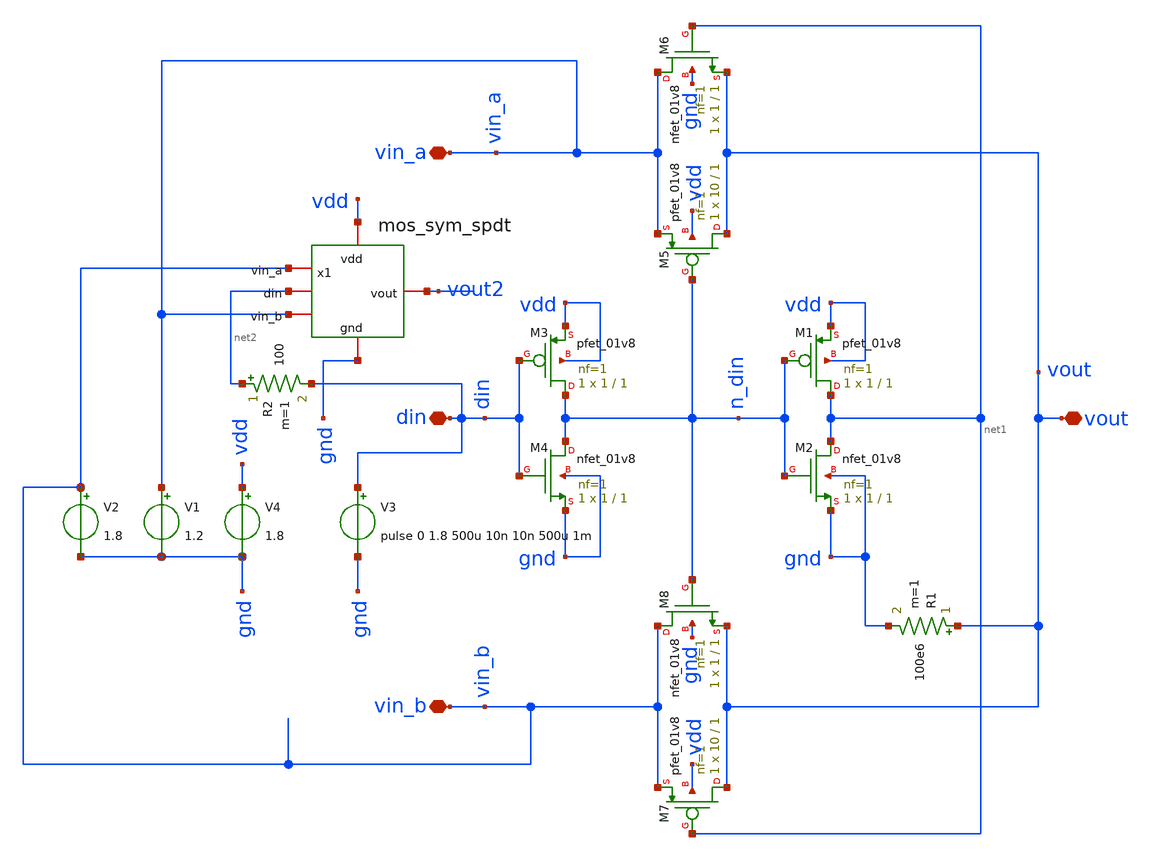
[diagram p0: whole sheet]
** sch_path: Schematics/mos_spdt.sch
**.subckt mos_spdt vout vin_a vin_b din
*.iopin vout
*.iopin vin_a
*.iopin vin_b
*.iopin din
XM3 n_din din vdd vdd sky130_fd_pr__pfet_01v8 L=1 W=1 nf=1 ad='int((nf+1)/2) * W/nf * 0.29' as='int((nf+2)/2) * W/nf * 0.29'
+ pd='2*int((nf+1)/2) * (W/nf + 0.29)' ps='2*int((nf+2)/2) * (W/nf + 0.29)' nrd='0.29 / W' nrs='0.29 / W'
+ sa=0 sb=0 sd=0 mult=1 m=1
XM4 n_din din gnd gnd sky130_fd_pr__nfet_01v8 L=1 W=1 nf=1 ad='int((1 + 1)/2) * 1 / 1 * 0.29' as='int((1 + 2)/2) * 1 / 1 * 0.29'
+ pd='2*int((1 + 1)/2) * (1 / 1 + 0.29)' ps='2*int((1 + 2)/2) * (1 / 1 + 0.29)' nrd='0.29 / 1 ' nrs='0.29 / 1 '
+ sa=0 sb=0 sd=0 mult=1 m=1
XM1 net1 n_din vdd vdd sky130_fd_pr__pfet_01v8 L=1 W=1 nf=1 ad='int((nf+1)/2) * W/nf * 0.29' as='int((nf+2)/2) * W/nf * 0.29'
+ pd='2*int((nf+1)/2) * (W/nf + 0.29)' ps='2*int((nf+2)/2) * (W/nf + 0.29)' nrd='0.29 / W' nrs='0.29 / W'
+ sa=0 sb=0 sd=0 mult=1 m=1
XM2 net1 n_din gnd gnd sky130_fd_pr__nfet_01v8 L=1 W=1 nf=1 ad='int((1 + 1)/2) * 1 / 1 * 0.29' as='int((1 + 2)/2) * 1 / 1 * 0.29'
+ pd='2*int((1 + 1)/2) * (1 / 1 + 0.29)' ps='2*int((1 + 2)/2) * (1 / 1 + 0.29)' nrd='0.29 / 1 ' nrs='0.29 / 1 '
+ sa=0 sb=0 sd=0 mult=1 m=1
XM5 vout n_din vin_a vdd sky130_fd_pr__pfet_01v8 L=1 W=10 nf=1 ad='int((nf+1)/2) * W/nf * 0.29' as='int((nf+2)/2) * W/nf * 0.29'
+ pd='2*int((nf+1)/2) * (W/nf + 0.29)' ps='2*int((nf+2)/2) * (W/nf + 0.29)' nrd='0.29 / W' nrs='0.29 / W'
+ sa=0 sb=0 sd=0 mult=1 m=1
XM6 vin_a net1 vout gnd sky130_fd_pr__nfet_01v8 L=1 W=1 nf=1 ad='int((1 + 1)/2) * 1 / 1 * 0.29' as='int((1 + 2)/2) * 1 / 1 * 0.29'
+ pd='2*int((1 + 1)/2) * (1 / 1 + 0.29)' ps='2*int((1 + 2)/2) * (1 / 1 + 0.29)' nrd='0.29 / 1 ' nrs='0.29 / 1 '
+ sa=0 sb=0 sd=0 mult=1 m=1
XM7 vout net1 vin_b vdd sky130_fd_pr__pfet_01v8 L=1 W=10 nf=1 ad='int((nf+1)/2) * W/nf * 0.29' as='int((nf+2)/2) * W/nf * 0.29'
+ pd='2*int((nf+1)/2) * (W/nf + 0.29)' ps='2*int((nf+2)/2) * (W/nf + 0.29)' nrd='0.29 / W' nrs='0.29 / W'
+ sa=0 sb=0 sd=0 mult=1 m=1
XM8 vin_b n_din vout gnd sky130_fd_pr__nfet_01v8 L=1 W=1 nf=1 ad='int((1 + 1)/2) * 1 / 1 * 0.29' as='int((1 + 2)/2) * 1 / 1 * 0.29'
+ pd='2*int((1 + 1)/2) * (1 / 1 + 0.29)' ps='2*int((1 + 2)/2) * (1 / 1 + 0.29)' nrd='0.29 / 1 ' nrs='0.29 / 1 '
+ sa=0 sb=0 sd=0 mult=1 m=1
V3 din gnd pulse 0 1.8 500u 10n 10n 500u 1m
V4 vdd gnd 1.8
V1 vin_a gnd 1.2
V2 vin_b gnd 1.8
R1 vout gnd 100e6 m=1
x1 vdd vin_b vout2 net2 vin_a gnd mos_sym_spdt
R2 net2 din 100 m=1
**** begin user architecture code

** opencircuitdesign pdks install
.lib $::SKYWATER_MODELS/sky130.lib.spice tt


**** end user architecture code
**.ends

* expanding   symbol:  Symbols/mos_sym_spdt.sym # of pins=6
** sym_path: Symbols/mos_sym_spdt.sym
** sch_path: Symbols/mos_sym_spdt.sch
.subckt mos_sym_spdt vdd vin_a vout din vin_b gnd
*.iopin vout
*.iopin vin_a
*.iopin vin_b
*.iopin vdd
*.iopin gnd
*.ipin din
XM3 n_din din vdd vdd sky130_fd_pr__pfet_01v8 L=1 W=1 nf=1 ad='int((nf+1)/2) * W/nf * 0.29' as='int((nf+2)/2) * W/nf * 0.29'
+ pd='2*int((nf+1)/2) * (W/nf + 0.29)' ps='2*int((nf+2)/2) * (W/nf + 0.29)' nrd='0.29 / W' nrs='0.29 / W'
+ sa=0 sb=0 sd=0 mult=1 m=1
XM4 n_din din net1 net1 sky130_fd_pr__nfet_01v8 L=1 W=1 nf=1 ad='int((1 + 1)/2) * 1 / 1 * 0.29' as='int((1 + 2)/2) * 1 / 1 * 0.29'
+ pd='2*int((1 + 1)/2) * (1 / 1 + 0.29)' ps='2*int((1 + 2)/2) * (1 / 1 + 0.29)' nrd='0.29 / 1 ' nrs='0.29 / 1 '
+ sa=0 sb=0 sd=0 mult=1 m=1
XM1 net2 n_din vdd vdd sky130_fd_pr__pfet_01v8 L=1 W=1 nf=1 ad='int((nf+1)/2) * W/nf * 0.29' as='int((nf+2)/2) * W/nf * 0.29'
+ pd='2*int((nf+1)/2) * (W/nf + 0.29)' ps='2*int((nf+2)/2) * (W/nf + 0.29)' nrd='0.29 / W' nrs='0.29 / W'
+ sa=0 sb=0 sd=0 mult=1 m=1
XM2 net2 n_din gnd gnd sky130_fd_pr__nfet_01v8 L=1 W=1 nf=1 ad='int((1 + 1)/2) * 1 / 1 * 0.29' as='int((1 + 2)/2) * 1 / 1 * 0.29'
+ pd='2*int((1 + 1)/2) * (1 / 1 + 0.29)' ps='2*int((1 + 2)/2) * (1 / 1 + 0.29)' nrd='0.29 / 1 ' nrs='0.29 / 1 '
+ sa=0 sb=0 sd=0 mult=1 m=1
XM5 vout n_din vin_a vdd sky130_fd_pr__pfet_01v8 L=1 W=10 nf=1 ad='int((nf+1)/2) * W/nf * 0.29' as='int((nf+2)/2) * W/nf * 0.29'
+ pd='2*int((nf+1)/2) * (W/nf + 0.29)' ps='2*int((nf+2)/2) * (W/nf + 0.29)' nrd='0.29 / W' nrs='0.29 / W'
+ sa=0 sb=0 sd=0 mult=1 m=1
XM6 vin_a net2 vout gnd sky130_fd_pr__nfet_01v8 L=1 W=1 nf=1 ad='int((1 + 1)/2) * 1 / 1 * 0.29' as='int((1 + 2)/2) * 1 / 1 * 0.29'
+ pd='2*int((1 + 1)/2) * (1 / 1 + 0.29)' ps='2*int((1 + 2)/2) * (1 / 1 + 0.29)' nrd='0.29 / 1 ' nrs='0.29 / 1 '
+ sa=0 sb=0 sd=0 mult=1 m=1
XM7 vout net2 vin_b vdd sky130_fd_pr__pfet_01v8 L=1 W=10 nf=1 ad='int((nf+1)/2) * W/nf * 0.29' as='int((nf+2)/2) * W/nf * 0.29'
+ pd='2*int((nf+1)/2) * (W/nf + 0.29)' ps='2*int((nf+2)/2) * (W/nf + 0.29)' nrd='0.29 / W' nrs='0.29 / W'
+ sa=0 sb=0 sd=0 mult=1 m=1
XM8 vin_b n_din vout gnd sky130_fd_pr__nfet_01v8 L=1 W=1 nf=1 ad='int((1 + 1)/2) * 1 / 1 * 0.29' as='int((1 + 2)/2) * 1 / 1 * 0.29'
+ pd='2*int((1 + 1)/2) * (1 / 1 + 0.29)' ps='2*int((1 + 2)/2) * (1 / 1 + 0.29)' nrd='0.29 / 1 ' nrs='0.29 / 1 '
+ sa=0 sb=0 sd=0 mult=1 m=1
.ends

**** begin user architecture code

* .option SCALE=1e-6
.option method=gear seed=12
.control
save all
tran 0.1m 1m
write mos_spdt.raw
plot din n_din vout
.endc


**** end user architecture code
.end
